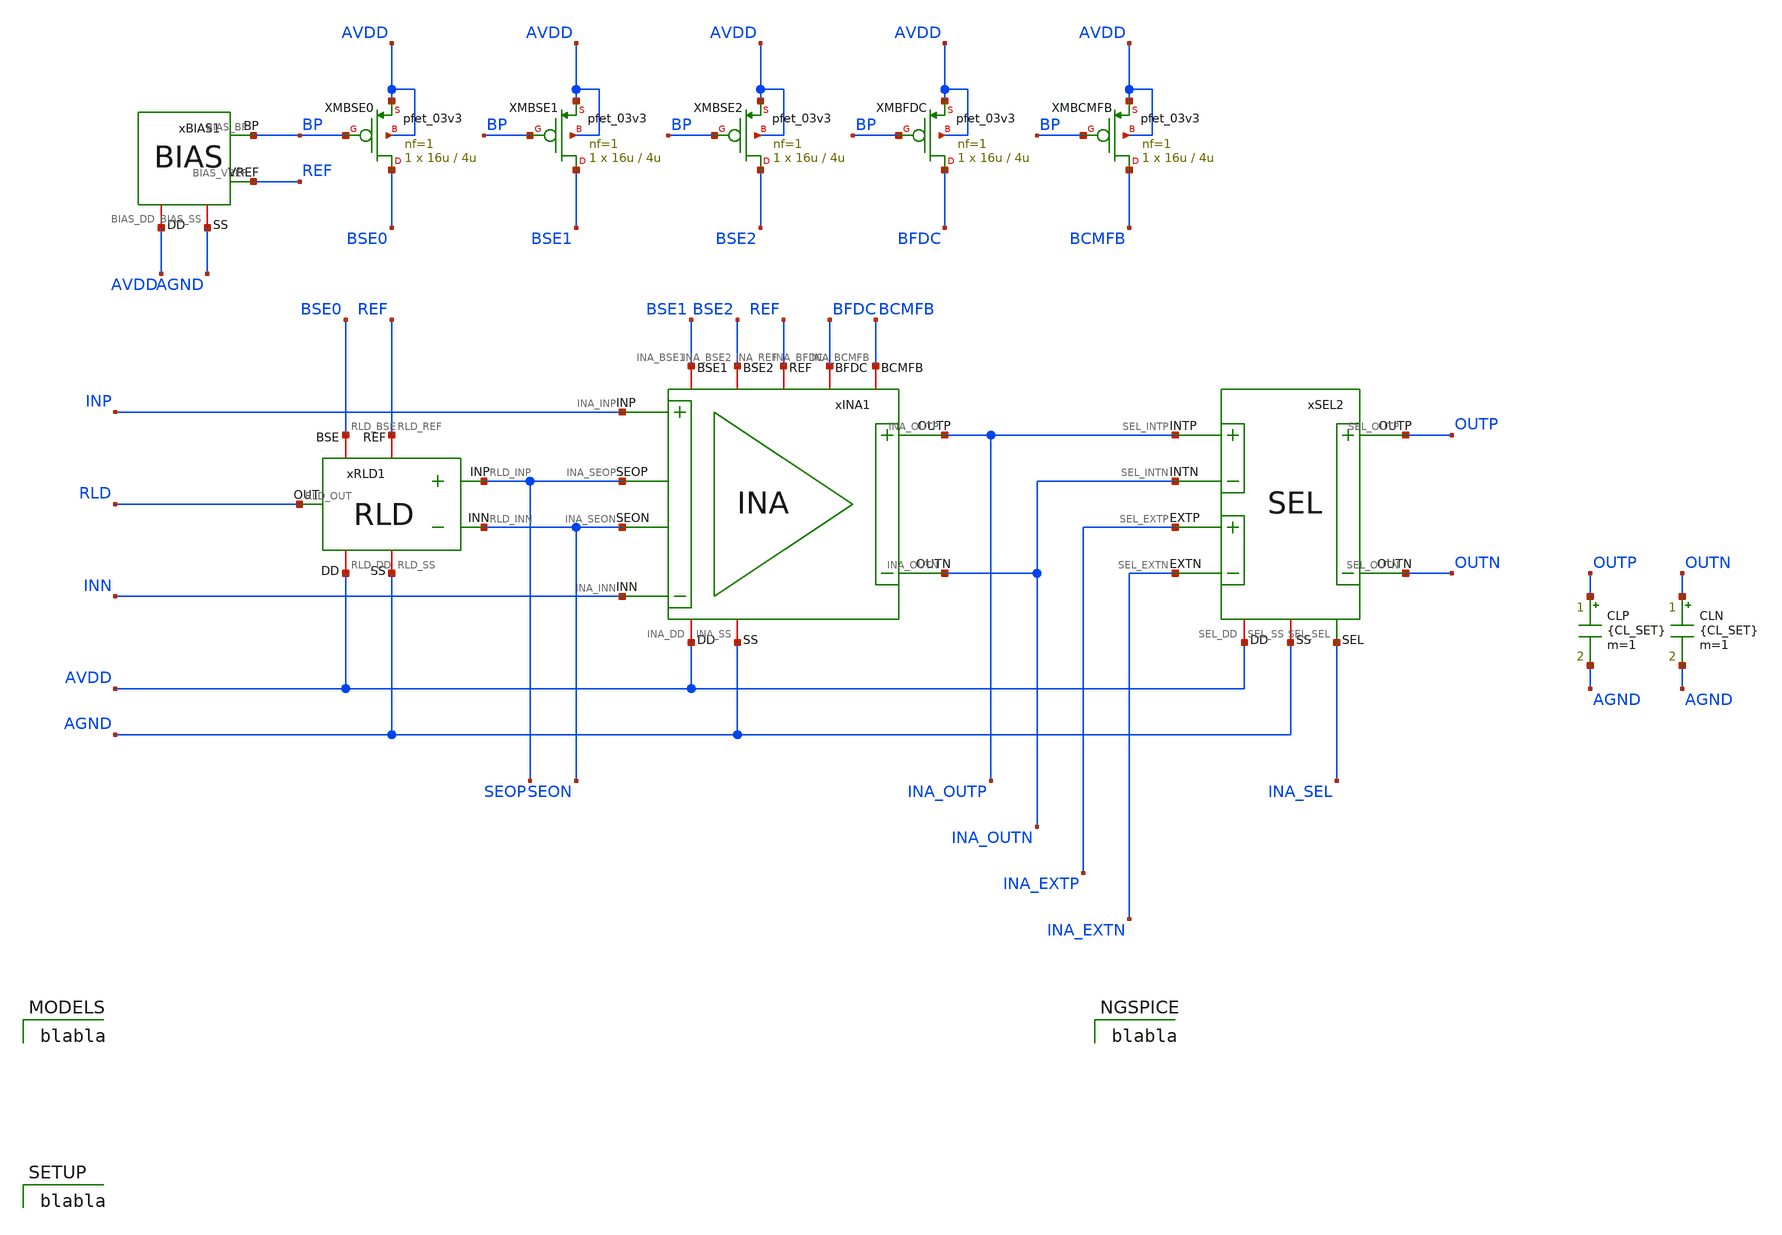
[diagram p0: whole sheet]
** sch_path: Design_Files/IC Design/Testbench/INA_RLD/INA_RLD_TB_NOM.sch
**.subckt INA_RLD_TB_NOM
xSEL2 AVDD AGND INA_OUTP INA_OUTN OUTN OUTP INA_EXTP INA_EXTN INA_SEL SEL
xINA1 AVDD AGND INP INN INA_OUTN BFDC INA_OUTP BCMFB REF SEON SEOP BSE1 BSE2 INA
xRLD1 AVDD AGND SEOP SEON RLD REF BSE0 RLD
CLP OUTP AGND {CL_SET} m=1
CLN OUTN AGND {CL_SET} m=1
xBIAS1 AVDD AGND BP REF BIAS
XMBSE0 BSE0 BP AVDD AVDD pfet_03v3 L=4u W=16u nf=1 ad='int((nf+1)/2) * W/nf * 0.18u' as='int((nf+2)/2) * W/nf * 0.18u'
+ pd='2*int((nf+1)/2) * (W/nf + 0.18u)' ps='2*int((nf+2)/2) * (W/nf + 0.18u)' nrd='0.18u / W' nrs='0.18u / W'
+ sa=0 sb=0 sd=0 m=1
XMBSE1 BSE1 BP AVDD AVDD pfet_03v3 L=4u W=16u nf=1 ad='int((nf+1)/2) * W/nf * 0.18u' as='int((nf+2)/2) * W/nf * 0.18u'
+ pd='2*int((nf+1)/2) * (W/nf + 0.18u)' ps='2*int((nf+2)/2) * (W/nf + 0.18u)' nrd='0.18u / W' nrs='0.18u / W'
+ sa=0 sb=0 sd=0 m=1
XMBSE2 BSE2 BP AVDD AVDD pfet_03v3 L=4u W=16u nf=1 ad='int((nf+1)/2) * W/nf * 0.18u' as='int((nf+2)/2) * W/nf * 0.18u'
+ pd='2*int((nf+1)/2) * (W/nf + 0.18u)' ps='2*int((nf+2)/2) * (W/nf + 0.18u)' nrd='0.18u / W' nrs='0.18u / W'
+ sa=0 sb=0 sd=0 m=1
XMBFDC BFDC BP AVDD AVDD pfet_03v3 L=4u W=16u nf=1 ad='int((nf+1)/2) * W/nf * 0.18u' as='int((nf+2)/2) * W/nf * 0.18u'
+ pd='2*int((nf+1)/2) * (W/nf + 0.18u)' ps='2*int((nf+2)/2) * (W/nf + 0.18u)' nrd='0.18u / W' nrs='0.18u / W'
+ sa=0 sb=0 sd=0 m=1
XMBCMFB BCMFB BP AVDD AVDD pfet_03v3 L=4u W=16u nf=1 ad='int((nf+1)/2) * W/nf * 0.18u' as='int((nf+2)/2) * W/nf * 0.18u'
+ pd='2*int((nf+1)/2) * (W/nf + 0.18u)' ps='2*int((nf+2)/2) * (W/nf + 0.18u)' nrd='0.18u / W' nrs='0.18u / W'
+ sa=0 sb=0 sd=0 m=1
**** begin user architecture code
 blabla

blabla


blabla

**** end user architecture code
**.ends
.end
